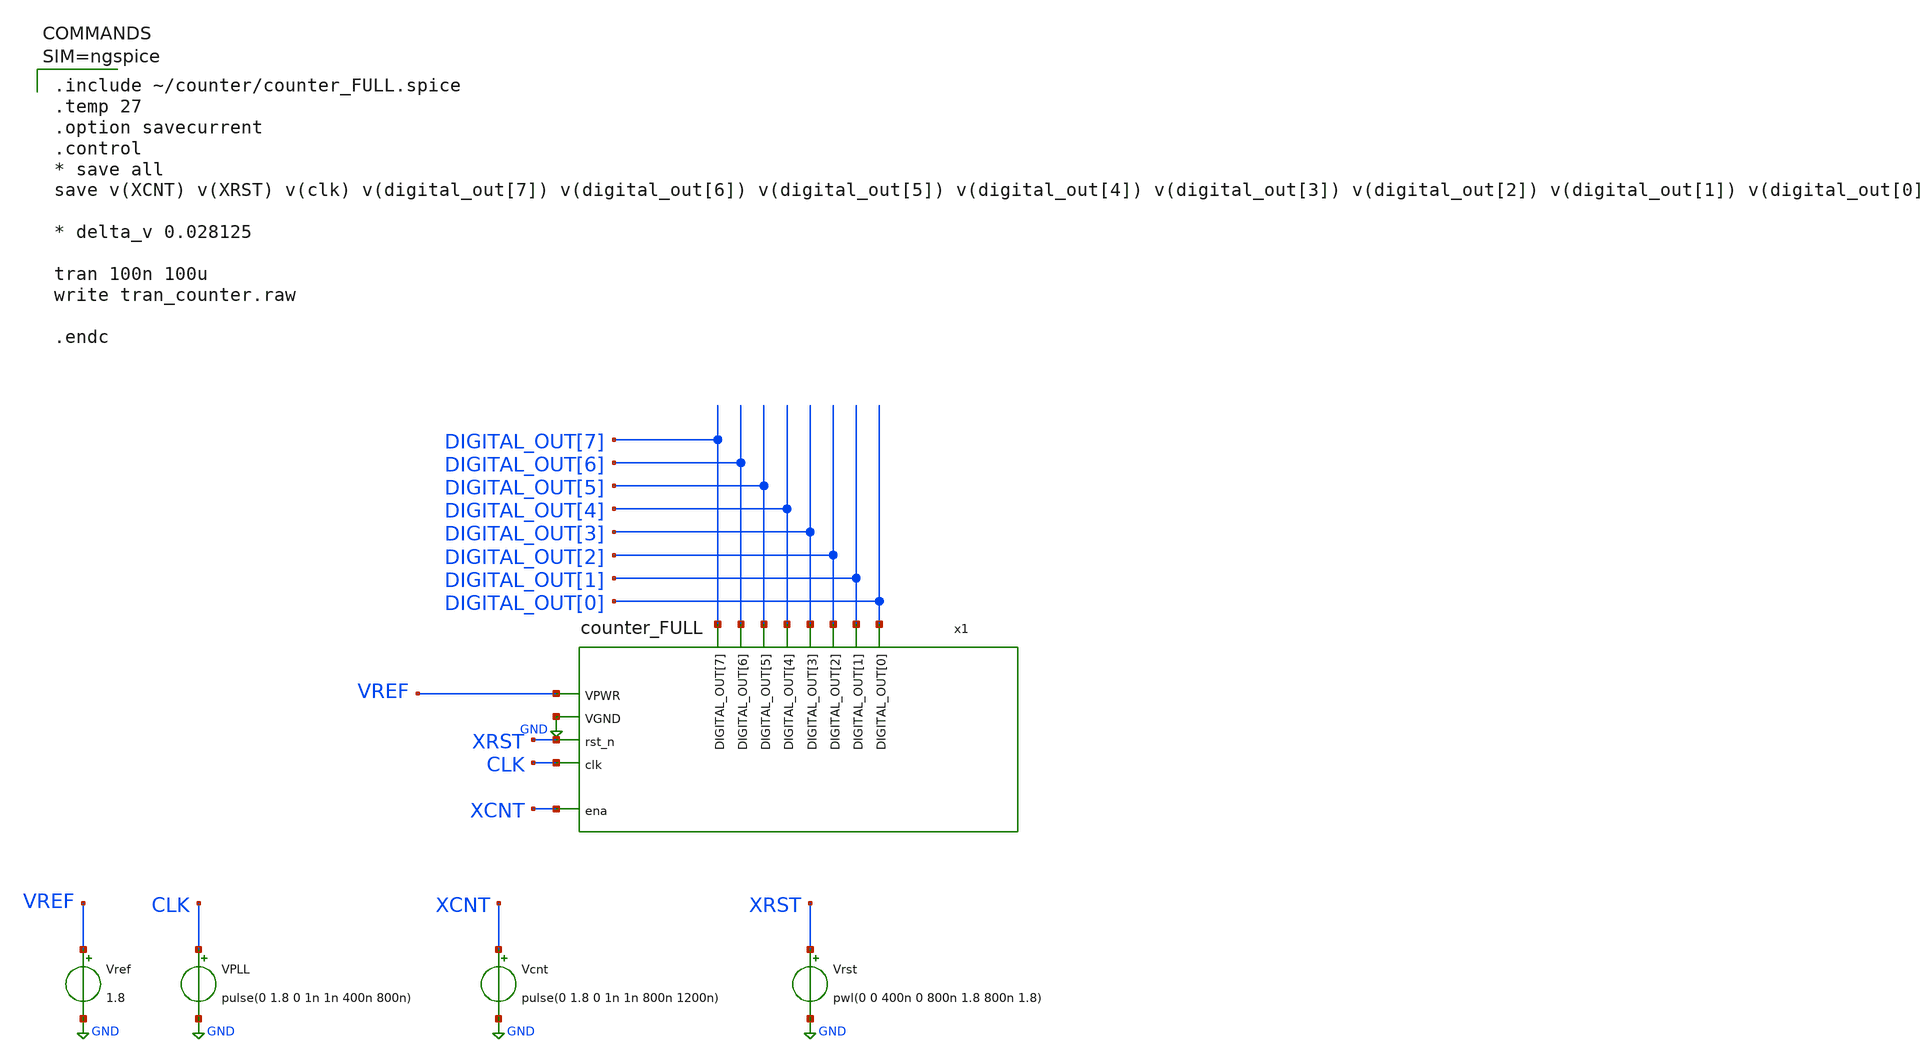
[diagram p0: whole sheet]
** sch_path: SKY130/SAR-ADC/8bit_counter/tran_counter.sch
**.subckt tran_counter
Vref VREF GND 1.8
VPLL CLK GND pulse(0 1.8 0 1n 1n 400n 800n)
Vcnt XCNT GND pulse(0 1.8 0 1n 1n 800n 1200n)
x1 GND VREF CLK DIGITAL_OUT[0] DIGITAL_OUT[1] DIGITAL_OUT[2] DIGITAL_OUT[3] DIGITAL_OUT[4]
+ DIGITAL_OUT[5] DIGITAL_OUT[6] DIGITAL_OUT[7] XCNT XRST counter
Vrst XRST GND pwl(0 0 400n 0 800n 1.8 800n 1.8)
**** begin user architecture code


.include ~/counter/counter_FULL.spice
.temp 27
.option savecurrent
.control
* save all
save v(XCNT) v(XRST) v(clk) v(digital_out[7]) v(digital_out[6]) v(digital_out[5]) v(digital_out[4])
+ v(digital_out[3]) v(digital_out[2]) v(digital_out[1]) v(digital_out[0])

* delta_v 0.028125

tran 100n 100u
write tran_counter.raw

.endc




** opencircuitdesign pdks install
.lib $::SKYWATER_MODELS/sky130.lib.spice tt

**** end user architecture code
**.ends
.GLOBAL GND
.end
